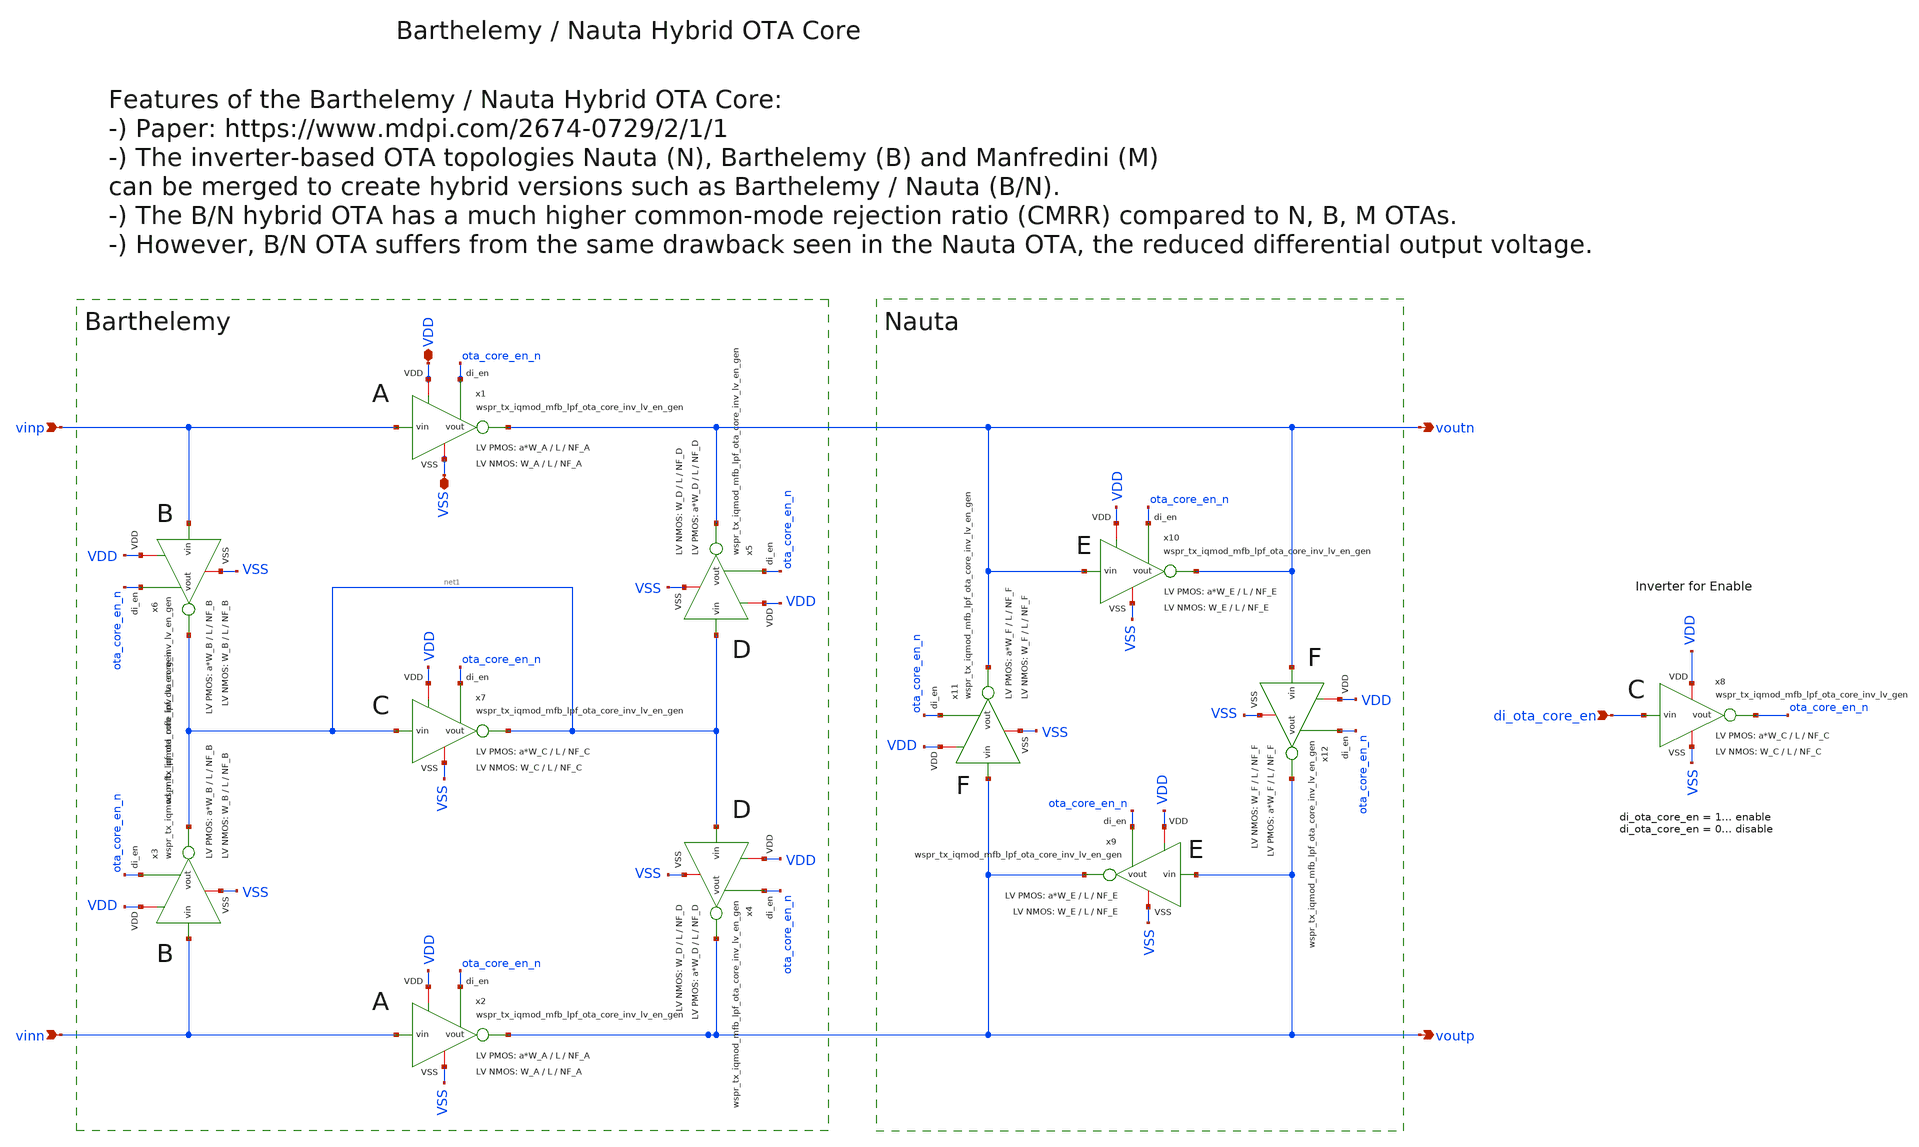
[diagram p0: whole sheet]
** sch_path: sky130/xschem/generic/wspr_tx_iqmod_mfb_lpf_ota_core_hybrid_bn_gen.sch
**.subckt wspr_tx_iqmod_mfb_lpf_ota_core_hybrid_bn_gen di_ota_core_en vinp vinn voutp voutn VDD VSS
*.ipin di_ota_core_en
*.ipin vinp
*.ipin vinn
*.opin voutp
*.opin voutn
*.iopin VDD
*.iopin VSS
x2 VDD vinn voutp VSS ota_core_en_n wspr_tx_iqmod_mfb_lpf_ota_core_inv_lv_en_gen W_P=a*W_A L_P=L
+ NF_P=NF_A W_N=W_A L_N=L NF_N=NF_A
x1 VDD vinp voutn VSS ota_core_en_n wspr_tx_iqmod_mfb_lpf_ota_core_inv_lv_en_gen W_P=a*W_A L_P=L
+ NF_P=NF_A W_N=W_A L_N=L NF_N=NF_A
x4 VDD net1 voutp VSS ota_core_en_n wspr_tx_iqmod_mfb_lpf_ota_core_inv_lv_en_gen W_P=a*W_D L_P=L
+ NF_P=NF_D W_N=W_D L_N=L NF_N=NF_D
x5 VDD net1 voutn VSS ota_core_en_n wspr_tx_iqmod_mfb_lpf_ota_core_inv_lv_en_gen W_P=a*W_D L_P=L
+ NF_P=NF_D W_N=W_D L_N=L NF_N=NF_D
x6 VDD vinp net1 VSS ota_core_en_n wspr_tx_iqmod_mfb_lpf_ota_core_inv_lv_en_gen W_P=a*W_B L_P=L
+ NF_P=NF_B W_N=W_B L_N=L NF_N=NF_B
x3 VDD vinn net1 VSS ota_core_en_n wspr_tx_iqmod_mfb_lpf_ota_core_inv_lv_en_gen W_P=a*W_B L_P=L
+ NF_P=NF_B W_N=W_B L_N=L NF_N=NF_B
x7 VDD net1 net1 VSS ota_core_en_n wspr_tx_iqmod_mfb_lpf_ota_core_inv_lv_en_gen W_P=a*W_C L_P=L
+ NF_P=NF_C W_N=W_C L_N=L NF_N=NF_C
x8 VDD di_ota_core_en ota_core_en_n VSS wspr_tx_iqmod_mfb_lpf_ota_core_inv_lv_gen W_P=a*W_C L_P=L
+ NF_P=NF_C W_N=W_C L_N=L NF_N=NF_C
x9 VDD voutp voutp VSS ota_core_en_n wspr_tx_iqmod_mfb_lpf_ota_core_inv_lv_en_gen W_P=a*W_E L_P=L
+ NF_P=NF_E W_N=W_E L_N=L NF_N=NF_E
x10 VDD voutn voutn VSS ota_core_en_n wspr_tx_iqmod_mfb_lpf_ota_core_inv_lv_en_gen W_P=a*W_E L_P=L
+ NF_P=NF_E W_N=W_E L_N=L NF_N=NF_E
x11 VDD voutp voutn VSS ota_core_en_n wspr_tx_iqmod_mfb_lpf_ota_core_inv_lv_en_gen W_P=a*W_F L_P=L
+ NF_P=NF_F W_N=W_F L_N=L NF_N=NF_F
x12 VDD voutn voutp VSS ota_core_en_n wspr_tx_iqmod_mfb_lpf_ota_core_inv_lv_en_gen W_P=a*W_F L_P=L
+ NF_P=NF_F W_N=W_F L_N=L NF_N=NF_F
**.ends
.end
